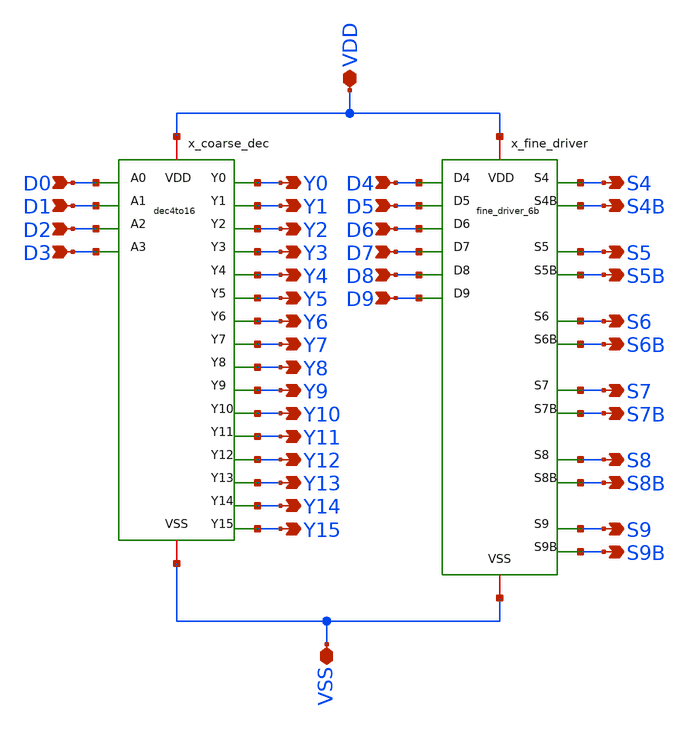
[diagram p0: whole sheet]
** sch_path: designs/archives/decoder_top_10b/decoder_top_10b.sch
**.subckt decoder_top_10b D0 D1 D2 D3 D4 D5 D6 D7 D8 D9 Y0 Y1 Y2 Y3 Y4 Y5 Y6 Y7 Y8 Y9 Y10 Y11 Y12
*+ Y13 Y14 Y15 S4 S4B S5 S5B S6 S6B S7 S7B S8 S8B S9 S9B VDD VSS
*.ipin D0
*.ipin D1
*.ipin D2
*.ipin D3
*.ipin D4
*.ipin D5
*.ipin D6
*.ipin D7
*.ipin D8
*.ipin D9
*.opin Y0
*.opin Y1
*.opin Y2
*.opin Y3
*.opin Y4
*.opin Y5
*.opin Y6
*.opin Y7
*.opin Y8
*.opin Y9
*.opin Y10
*.opin Y11
*.opin Y12
*.opin Y13
*.opin Y14
*.opin Y15
*.opin S4
*.opin S4B
*.opin S5
*.opin S5B
*.opin S6
*.opin S6B
*.opin S7
*.opin S7B
*.opin S8
*.opin S8B
*.opin S9
*.opin S9B
*.iopin VDD
*.iopin VSS
x_coarse_dec D0 D3 Y0 Y1 Y2 Y3 VDD VSS Y4 Y5 Y6 Y7 Y8 Y9 Y10 Y11 Y12 Y13 Y14 Y15 D1 D2 dec4to16
x_fine_driver D4 D7 S4 S4B VDD VSS D5 D6 D8 D9 S5 S5B S6 S6B S7 S7B S8 S8B S9 S9B fine_driver_6b
**.ends
.end
